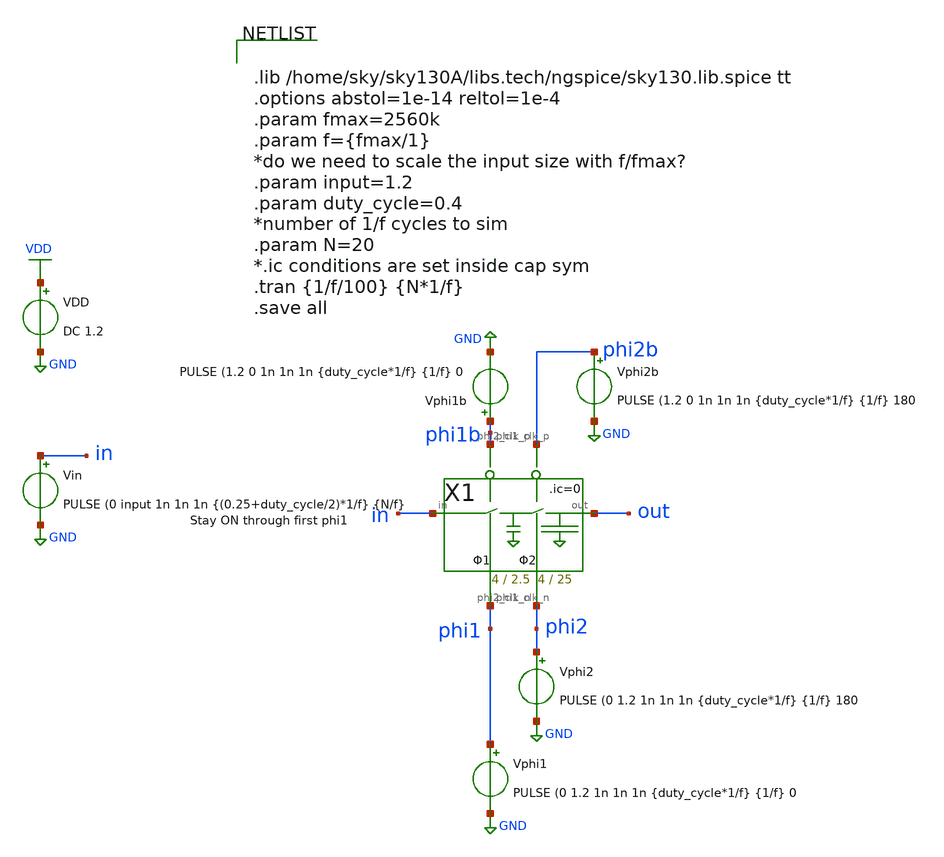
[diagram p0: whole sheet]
** sch_path: xschem/Switched_Caps/2switchcaps_tb.sch
**.subckt 2switchcaps_tb
Vin in GND PULSE (0 input 1n 1n 1n {(0.25+duty_cycle/2)*1/f} {N/f}
X1 in out phi2 phi1 phi1b phi2b 2switchcaps Wcap1=4 Lcap1=2.5 Wcap2=4 Lcap2=25
VDD VDD GND DC 1.2
Vphi1 phi1 GND PULSE (0 1.2 1n 1n 1n {duty_cycle*1/f} {1/f} 0
Vphi1b phi1b GND PULSE (1.2 0 1n 1n 1n {duty_cycle*1/f} {1/f} 0
Vphi2 phi2 GND PULSE (0 1.2 1n 1n 1n {duty_cycle*1/f} {1/f} 180
Vphi2b phi2b GND PULSE (1.2 0 1n 1n 1n {duty_cycle*1/f} {1/f} 180
**** begin user architecture code


.lib /home/sky/sky130A/libs.tech/ngspice/sky130.lib.spice tt
.options abstol=1e-14 reltol=1e-4
.param fmax=2560k
.param f={fmax/1}
*do we need to scale the input size with f/fmax?
.param input=1.2
.param duty_cycle=0.4
*number of 1/f cycles to sim
.param N=20
*.ic conditions are set inside cap sym
.tran {1/f/100} {N*1/f}
.save all


**** end user architecture code
**.ends

* expanding   symbol:  Switched_Caps/2switchcaps.sym # of pins=6
** sym_path: xschem/Switched_Caps/2switchcaps.sym
** sch_path: xschem/Switched_Caps/2switchcaps.sch
.subckt 2switchcaps in out phi2_clk_n phi1_clk_n phi1_clk_p phi2_clk_p  Wcap1=4 Lcap1=2.5 Wcap2=4
+ Lcap2=25
*.iopin out
*.iopin in
*.ipin phi1_clk_n
*.ipin phi1_clk_p
*.ipin phi2_clk_p
*.ipin phi2_clk_n
XC1 c1 GND sky130_fd_pr__cap_mim_m3_1 W=Wcap1 L=Lcap1 MF=1 m=1
XC2 out GND sky130_fd_pr__cap_mim_m3_1 W=Wcap2 L=Lcap2 MF=1 m=1
**** begin user architecture code

.ic v(c1)=0 v(out)=0

**** end user architecture code
X1 in c1 phi1_clk_p phi1_clk_n transmission_gate Wpmos=0.42 Lpmos=0.18 Wnmos=0.42 Lnmos=0.18
X2 c1 out phi2_clk_p phi2_clk_n transmission_gate Wpmos=0.42 Lpmos=0.18 Wnmos=0.42 Lnmos=0.18
.ends


* expanding   symbol:  transmission_gate/transmission_gate.sym # of pins=4
** sym_path: xschem/transmission_gate/transmission_gate.sym
** sch_path: xschem/transmission_gate/transmission_gate.sch
.subckt transmission_gate in out ctrl_ ctrl  Wpmos=0.42 Lpmos=0.18 Wnmos=0.42 Lnmos=0.18
*.iopin in
*.iopin out
*.ipin ctrl_
*.ipin ctrl
XM1 out ctrl in GND sky130_fd_pr__nfet_01v8 L=Lnmos W=Wnmos nf=1 ad='int((nf+1)/2) * W/nf * 0.29' as='int((nf+2)/2) * W/nf * 0.29'
+ pd='2*int((nf+1)/2) * (W/nf + 0.29)' ps='2*int((nf+2)/2) * (W/nf + 0.29)' nrd='0.29 / W' nrs='0.29 / W'
+ sa=0 sb=0 sd=0 mult=1 m=1
XM2 out ctrl_ in VDD sky130_fd_pr__pfet_01v8 L=Lpmos W=Wpmos nf=1 ad='int((nf+1)/2) * W/nf * 0.29' as='int((nf+2)/2) * W/nf * 0.29'
+ pd='2*int((nf+1)/2) * (W/nf + 0.29)' ps='2*int((nf+2)/2) * (W/nf + 0.29)' nrd='0.29 / W' nrs='0.29 / W'
+ sa=0 sb=0 sd=0 mult=1 m=1
.ends

.GLOBAL GND
.GLOBAL VDD
.end
